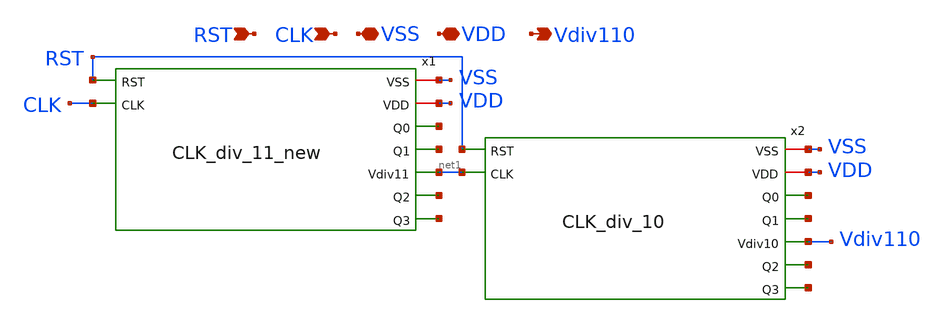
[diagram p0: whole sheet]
** sch_path: Clock_Generator_PAKISTAN_02/Schematics/CLK_div_110.sch
**.subckt CLK_div_110 CLK VSS VDD RST Vdiv110
*.ipin CLK
*.iopin VSS
*.iopin VDD
*.ipin RST
*.opin Vdiv110
x2 VSS VDD net2 net3 RST Vdiv110 net4 net5 net1 CLK_div_10
x1 VSS VDD net6 net7 RST net1 net8 net9 CLK CLK_div_11_new
**.ends
.end
